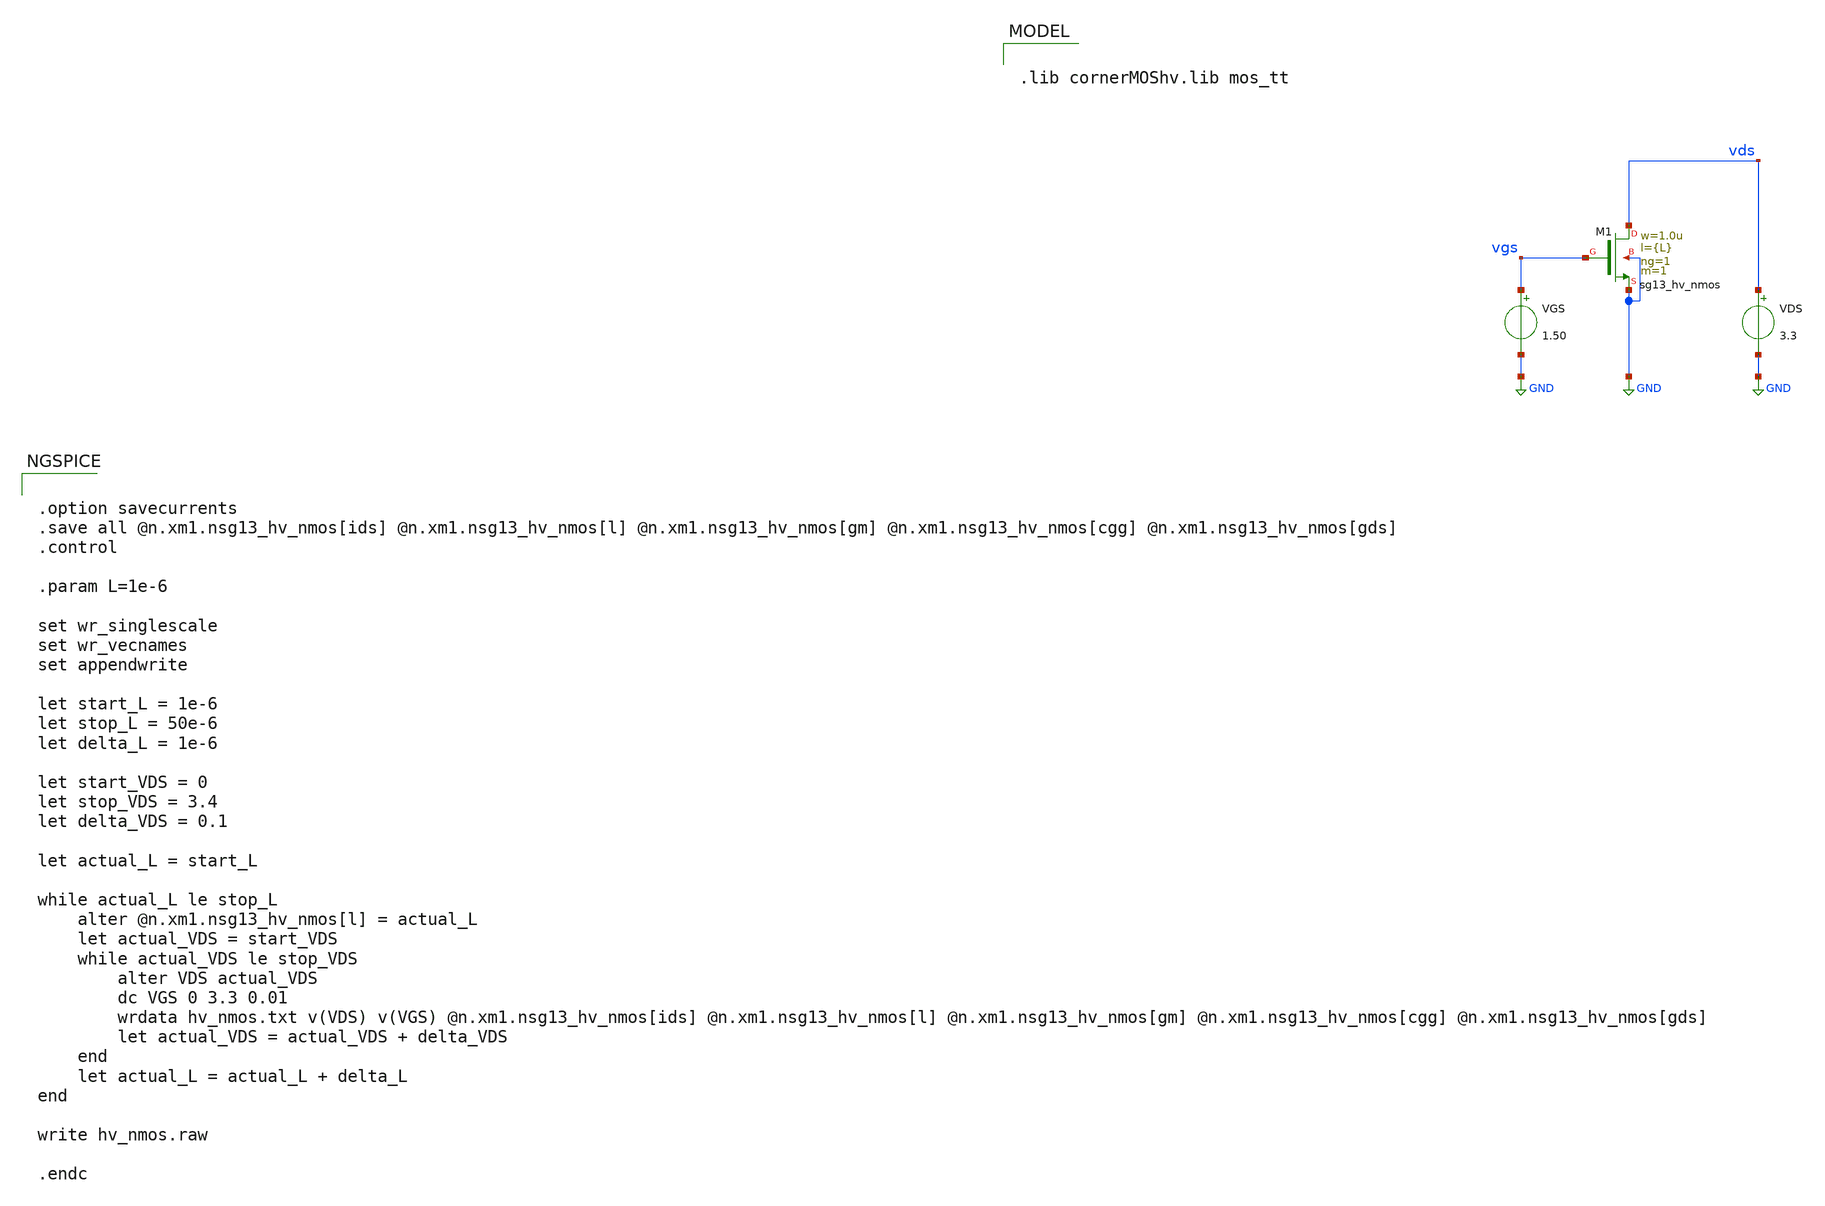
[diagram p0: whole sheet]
** sch_path: gmid/hv_nmos.sch
**.subckt hv_nmos
XM1 vds vgs GND GND sg13_hv_nmos w=1.0u l={L} ng=1 m=1 mm_ok=1
VGS vgs GND 1.50
VDS vds GND 3.3
**** begin user architecture code

.lib cornerMOShv.lib mos_tt



.option savecurrents
.save all @n.xm1.nsg13_hv_nmos[ids] @n.xm1.nsg13_hv_nmos[l] @n.xm1.nsg13_hv_nmos[gm] @n.xm1.nsg13_hv_nmos[cgg] @n.xm1.nsg13_hv_nmos[gds]
.control

.param L=1e-6

set wr_singlescale
set wr_vecnames
set appendwrite

let start_L = 1e-6
let stop_L = 50e-6
let delta_L = 1e-6

let start_VDS = 0
let stop_VDS = 3.4
let delta_VDS = 0.1

let actual_L = start_L

while actual_L le stop_L
	alter @n.xm1.nsg13_hv_nmos[l] = actual_L
	let actual_VDS = start_VDS
	while actual_VDS le stop_VDS
		alter VDS actual_VDS
		dc VGS 0 3.3 0.01
		wrdata hv_nmos.txt v(VDS) v(VGS) @n.xm1.nsg13_hv_nmos[ids] @n.xm1.nsg13_hv_nmos[l]
+ @n.xm1.nsg13_hv_nmos[gm] @n.xm1.nsg13_hv_nmos[cgg] @n.xm1.nsg13_hv_nmos[gds]
		let actual_VDS = actual_VDS + delta_VDS
	end
	let actual_L = actual_L + delta_L
end

write hv_nmos.raw

.endc



**** end user architecture code
**.ends
.GLOBAL GND
.end
